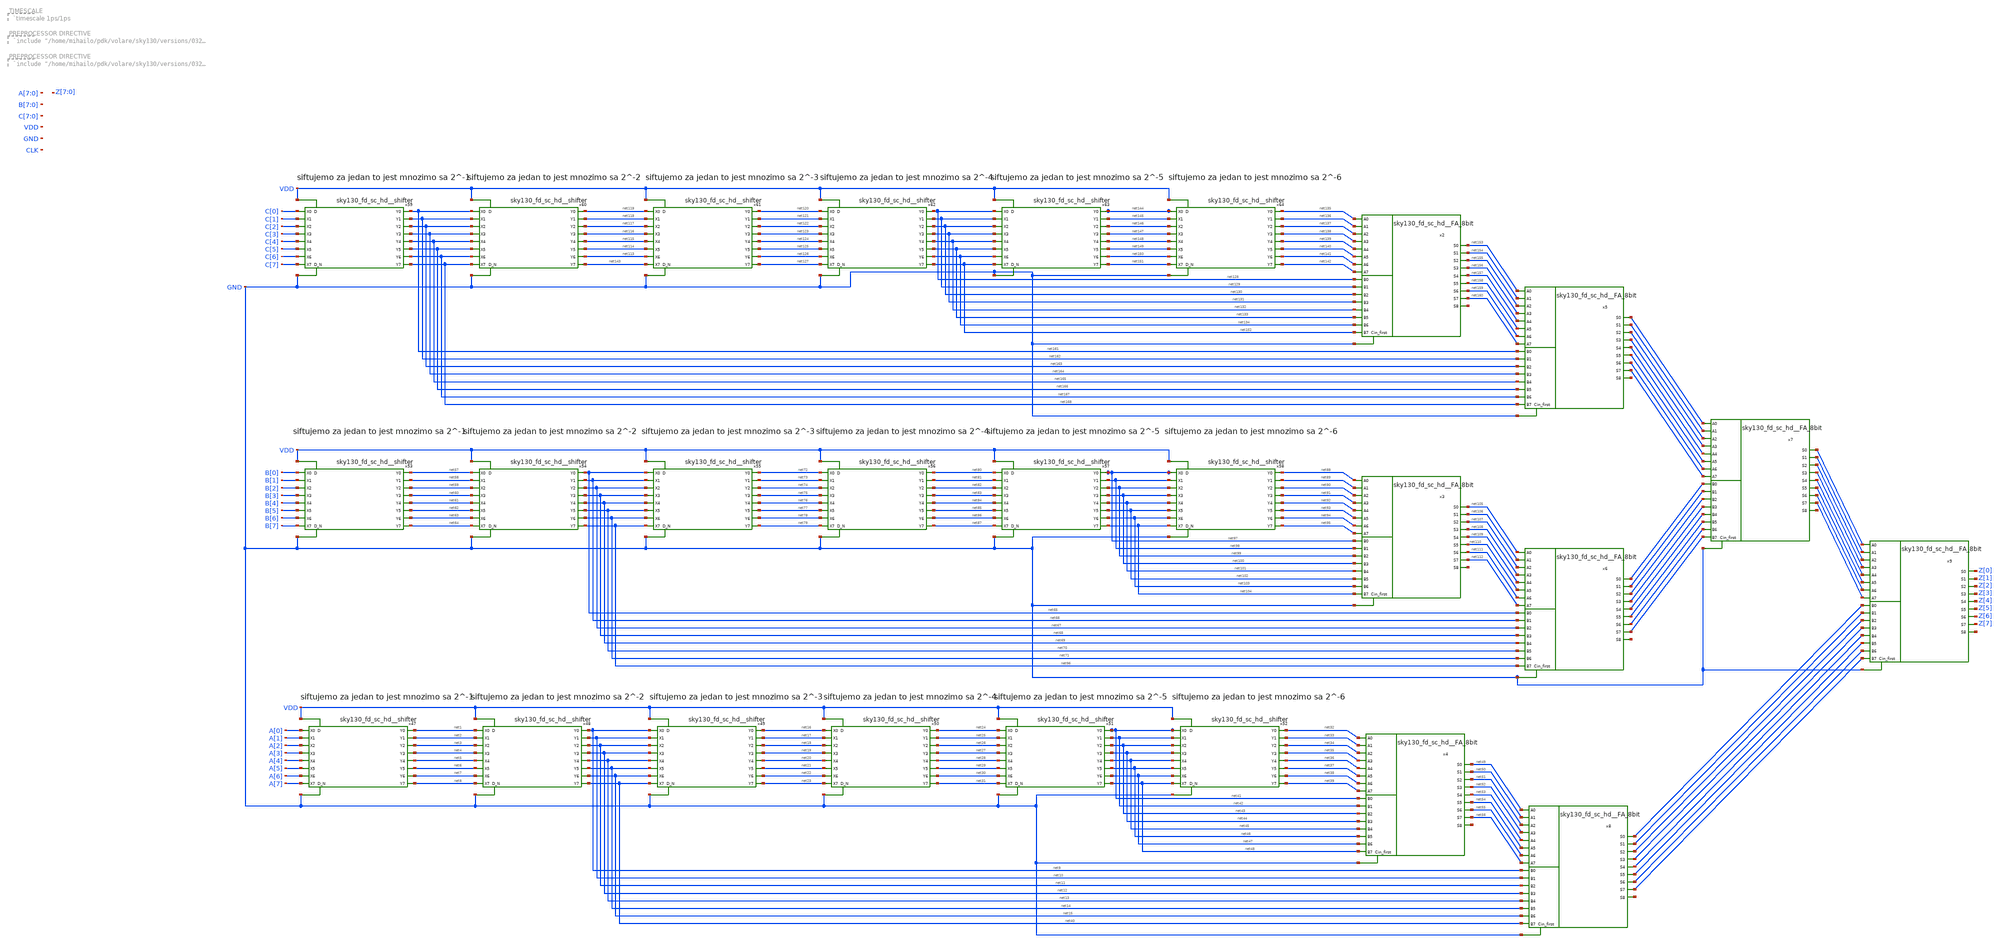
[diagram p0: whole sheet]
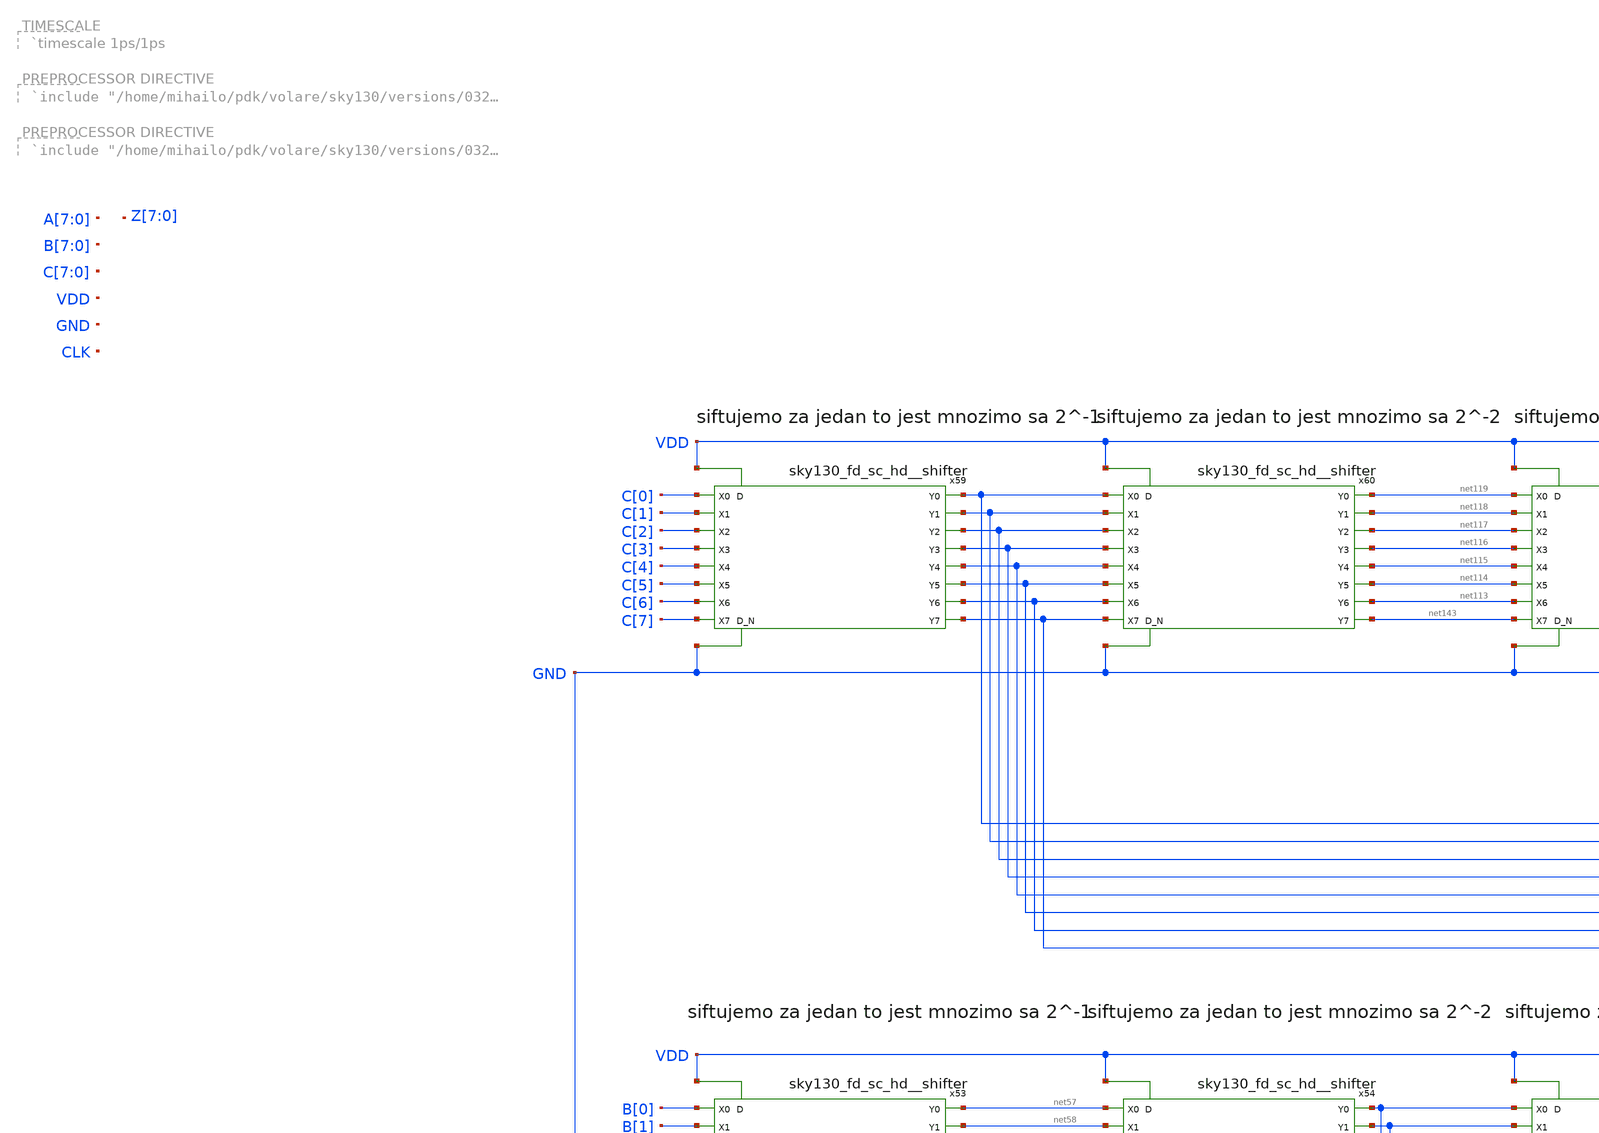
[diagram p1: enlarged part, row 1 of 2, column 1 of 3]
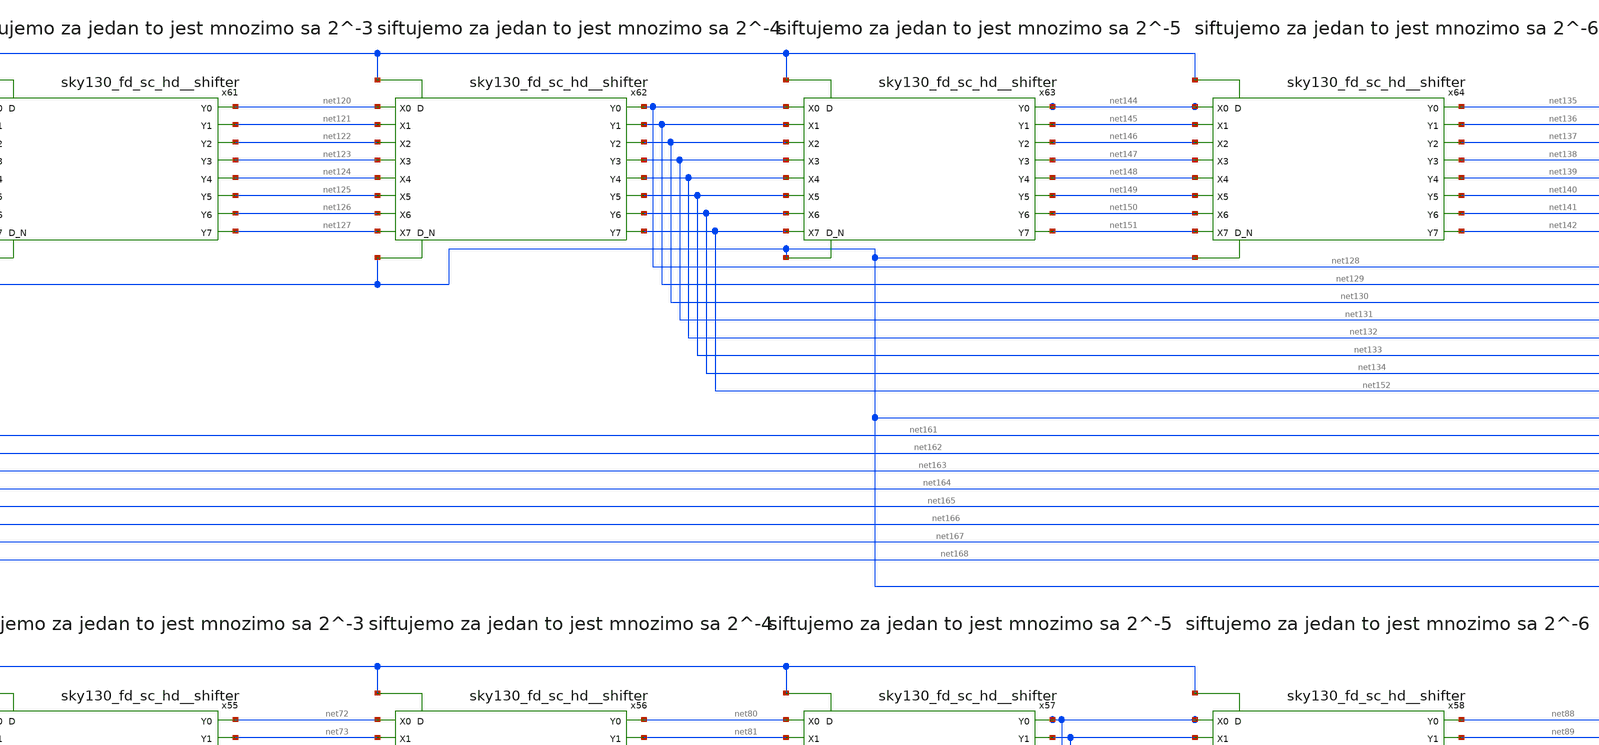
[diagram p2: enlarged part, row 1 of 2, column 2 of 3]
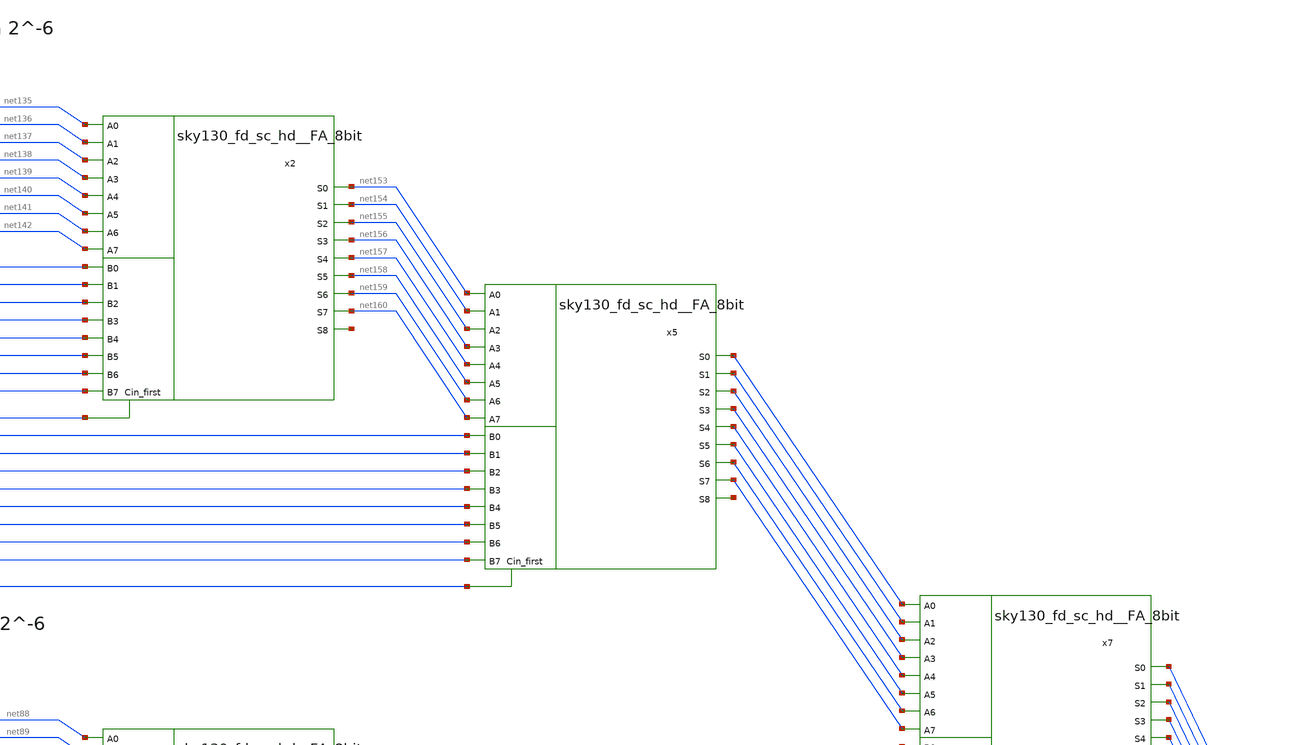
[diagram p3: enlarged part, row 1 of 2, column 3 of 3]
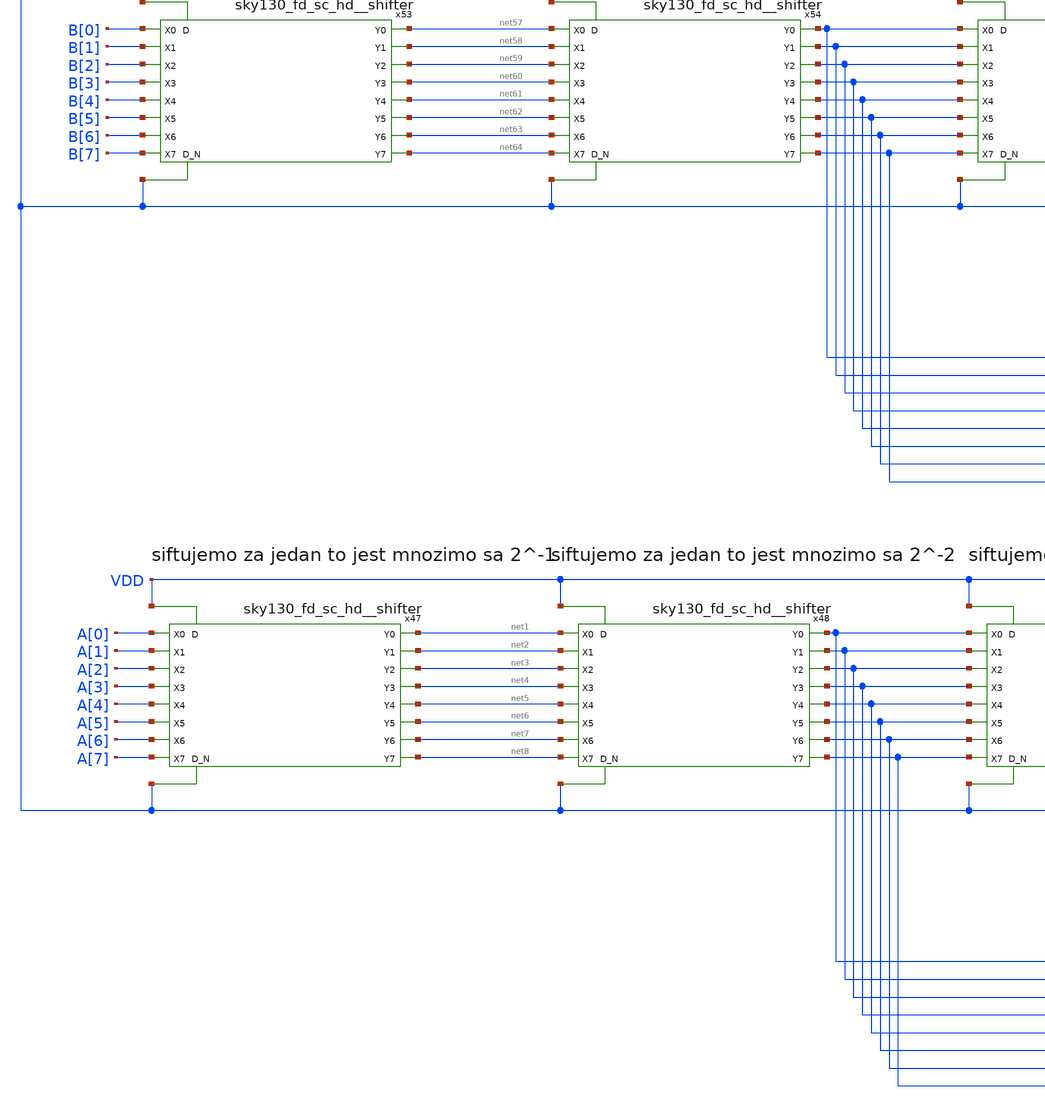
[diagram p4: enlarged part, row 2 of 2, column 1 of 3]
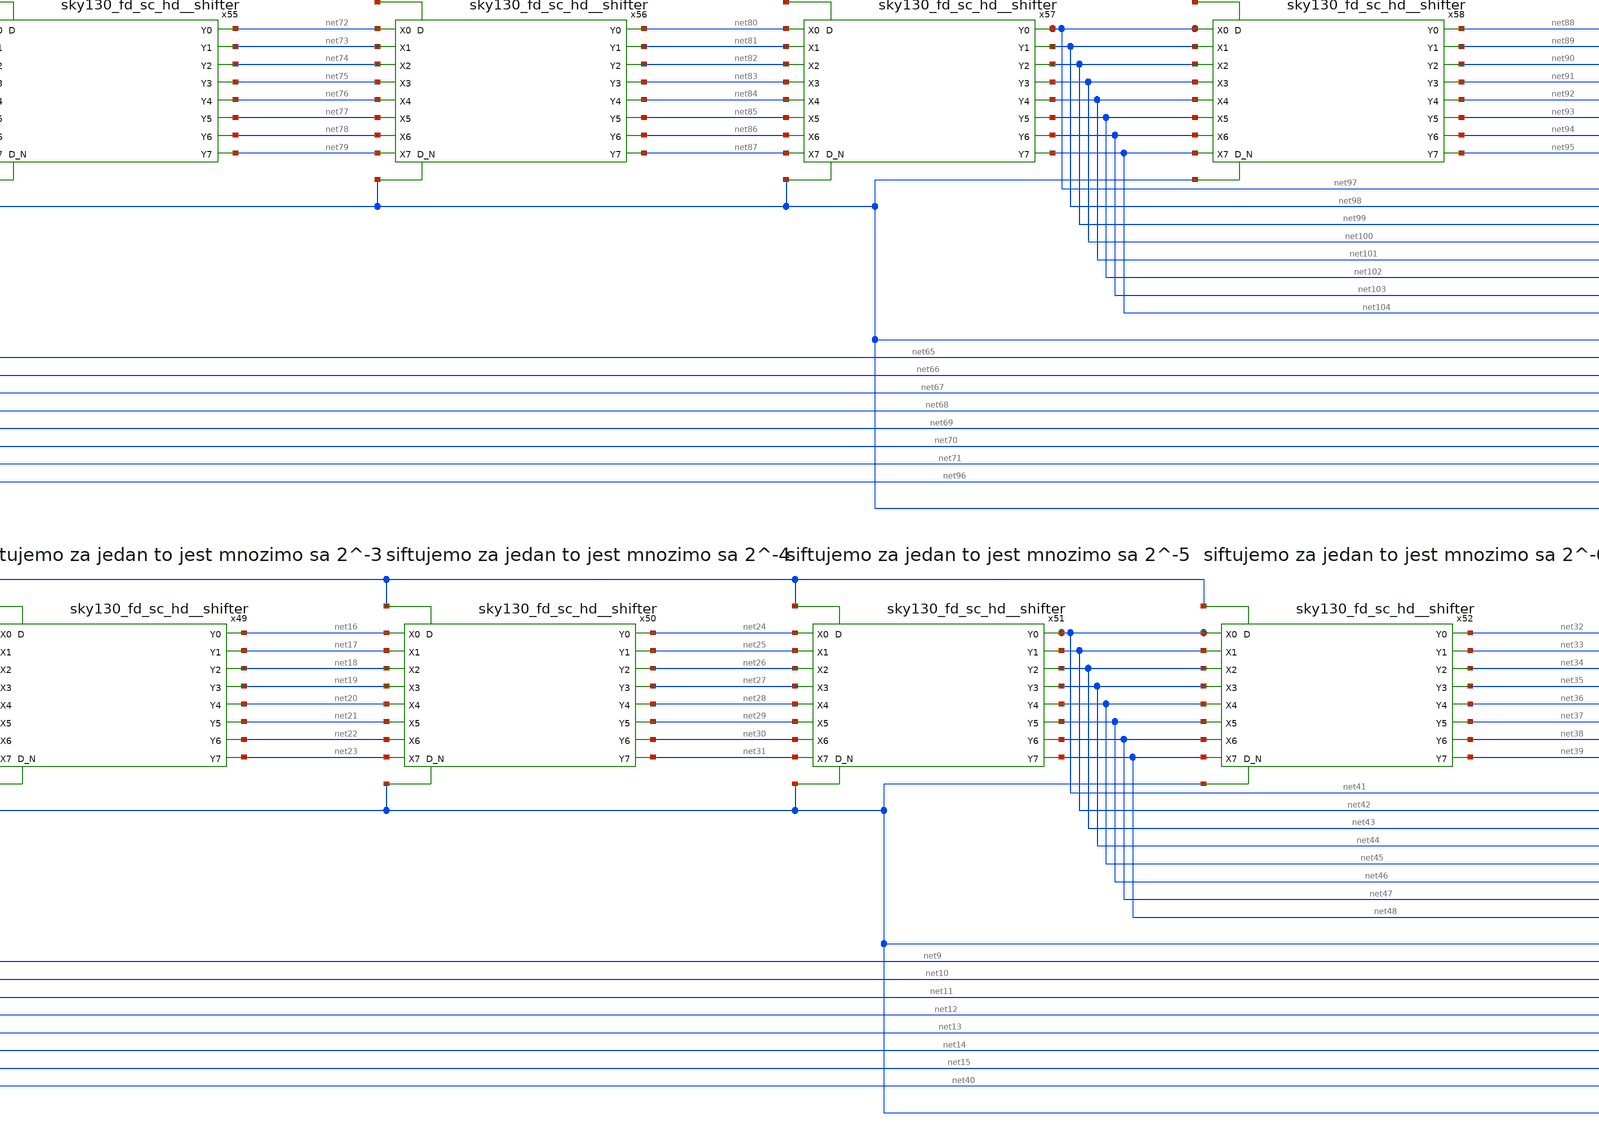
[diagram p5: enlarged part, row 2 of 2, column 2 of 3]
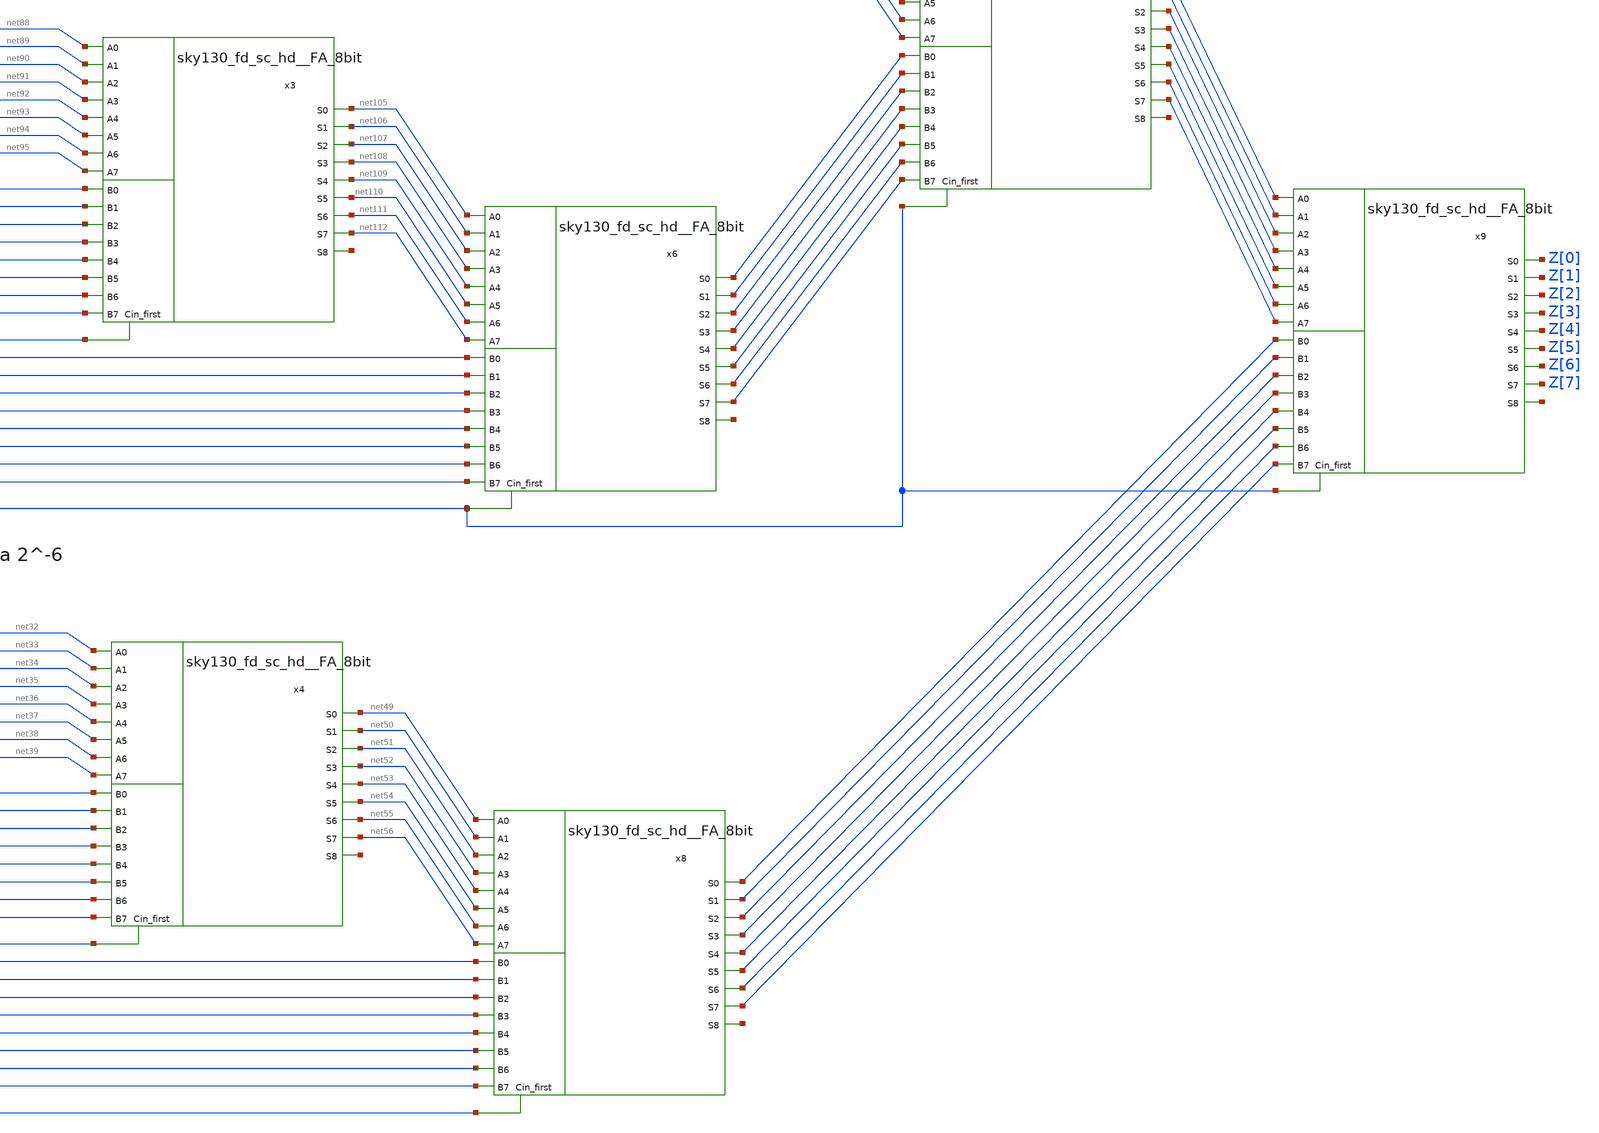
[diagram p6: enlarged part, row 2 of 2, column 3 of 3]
** sch_path: projekat_spice/xschem/fir_filter_verilog.sch
**.subckt fir_filter_verilog
x47 A[0] net1 net2 A[1] net3 A[2] A[3] net4 net5 A[4] A[5] net6 net7 A[6] net8 A[7] VDD GND
+ sky130_fd_sc_hd__shifter
x48 net1 net9 net10 net2 net11 net3 net4 net12 net13 net5 net6 net14 net15 net7 net40 net8 VDD GND
+ sky130_fd_sc_hd__shifter
x49 net9 net16 net17 net10 net18 net11 net12 net19 net20 net13 net14 net21 net22 net15 net23 net40
+ VDD GND sky130_fd_sc_hd__shifter
x50 net16 net24 net25 net17 net26 net18 net19 net27 net28 net20 net21 net29 net30 net22 net31 net23
+ VDD GND sky130_fd_sc_hd__shifter
x51 net24 net41 net42 net25 net43 net26 net27 net44 net45 net28 net29 net46 net47 net30 net48 net31
+ VDD GND sky130_fd_sc_hd__shifter
x52 net41 net32 net33 net42 net34 net43 net44 net35 net36 net45 net46 net37 net38 net47 net39 net48
+ VDD GND sky130_fd_sc_hd__shifter
x53 B[0] net57 net58 B[1] net59 B[2] B[3] net60 net61 B[4] B[5] net62 net63 B[6] net64 B[7] VDD GND
+ sky130_fd_sc_hd__shifter
x54 net57 net65 net66 net58 net67 net59 net60 net68 net69 net61 net62 net70 net71 net63 net96 net64
+ VDD GND sky130_fd_sc_hd__shifter
x55 net65 net72 net73 net66 net74 net67 net68 net75 net76 net69 net70 net77 net78 net71 net79 net96
+ VDD GND sky130_fd_sc_hd__shifter
x56 net72 net80 net81 net73 net82 net74 net75 net83 net84 net76 net77 net85 net86 net78 net87 net79
+ VDD GND sky130_fd_sc_hd__shifter
x57 net80 net97 net98 net81 net99 net82 net83 net100 net101 net84 net85 net102 net103 net86 net104
+ net87 VDD GND sky130_fd_sc_hd__shifter
x58 net97 net88 net89 net98 net90 net99 net100 net91 net92 net101 net102 net93 net94 net103 net95
+ net104 VDD GND sky130_fd_sc_hd__shifter
x59 C[0] net161 net162 C[1] net163 C[2] C[3] net164 net165 C[4] C[5] net166 net167 C[6] net168 C[7]
+ VDD GND sky130_fd_sc_hd__shifter
x60 net161 net119 net118 net162 net117 net163 net164 net116 net115 net165 net166 net114 net113
+ net167 net143 net168 VDD GND sky130_fd_sc_hd__shifter
x61 net119 net120 net121 net118 net122 net117 net116 net123 net124 net115 net114 net125 net126
+ net113 net127 net143 VDD GND sky130_fd_sc_hd__shifter
x62 net120 net128 net129 net121 net130 net122 net123 net131 net132 net124 net125 net133 net134
+ net126 net152 net127 VDD GND sky130_fd_sc_hd__shifter
x63 net128 net144 net145 net129 net146 net130 net131 net147 net148 net132 net133 net149 net150
+ net134 net151 net152 VDD GND sky130_fd_sc_hd__shifter
x64 net144 net135 net136 net145 net137 net146 net147 net138 net139 net148 net149 net140 net141
+ net150 net142 net151 VDD GND sky130_fd_sc_hd__shifter
x2 net128 net129 net130 net131 net132 net133 net134 net152 net135 net136 net137 net138 net139 net140
+ net141 net142 net153 net154 net155 net156 net157 net158 net159 net160 net201 GND sky130_fd_sc_hd__FA_8bit
x3 net97 net98 net99 net100 net101 net102 net103 net104 net88 net89 net90 net91 net92 net93 net94
+ net95 net105 net106 net107 net108 net109 net110 net111 net112 net202 GND sky130_fd_sc_hd__FA_8bit
x4 net41 net42 net43 net44 net45 net46 net47 net48 net32 net33 net34 net35 net36 net37 net38 net39
+ net49 net50 net51 net52 net53 net54 net55 net56 net203 GND sky130_fd_sc_hd__FA_8bit
x5 net161 net162 net163 net164 net165 net166 net167 net168 net153 net154 net155 net156 net157 net158
+ net159 net160 net169 net170 net172 net171 net173 net174 net175 net176 net204 GND sky130_fd_sc_hd__FA_8bit
x6 net65 net66 net67 net68 net69 net70 net71 net96 net105 net106 net107 net108 net109 net110 net111
+ net112 net177 net178 net179 net180 net181 net182 net183 net184 net205 GND sky130_fd_sc_hd__FA_8bit
x7 net177 net178 net179 net180 net181 net182 net183 net184 net169 net170 net172 net171 net173 net174
+ net175 net176 net193 net194 net195 net196 net197 net198 net199 net200 net206 GND sky130_fd_sc_hd__FA_8bit
x8 net9 net10 net11 net12 net13 net14 net15 net40 net49 net50 net51 net52 net53 net54 net55 net56
+ net185 net187 net186 net188 net189 net190 net191 net192 net207 GND sky130_fd_sc_hd__FA_8bit
x9 net185 net187 net186 net188 net189 net190 net191 net192 net193 net194 net195 net196 net197 net198
+ net199 net200 Z[0] Z[1] Z[2] Z[3] Z[4] Z[5] Z[6] Z[7] net208 GND sky130_fd_sc_hd__FA_8bit
**.ends
.end
